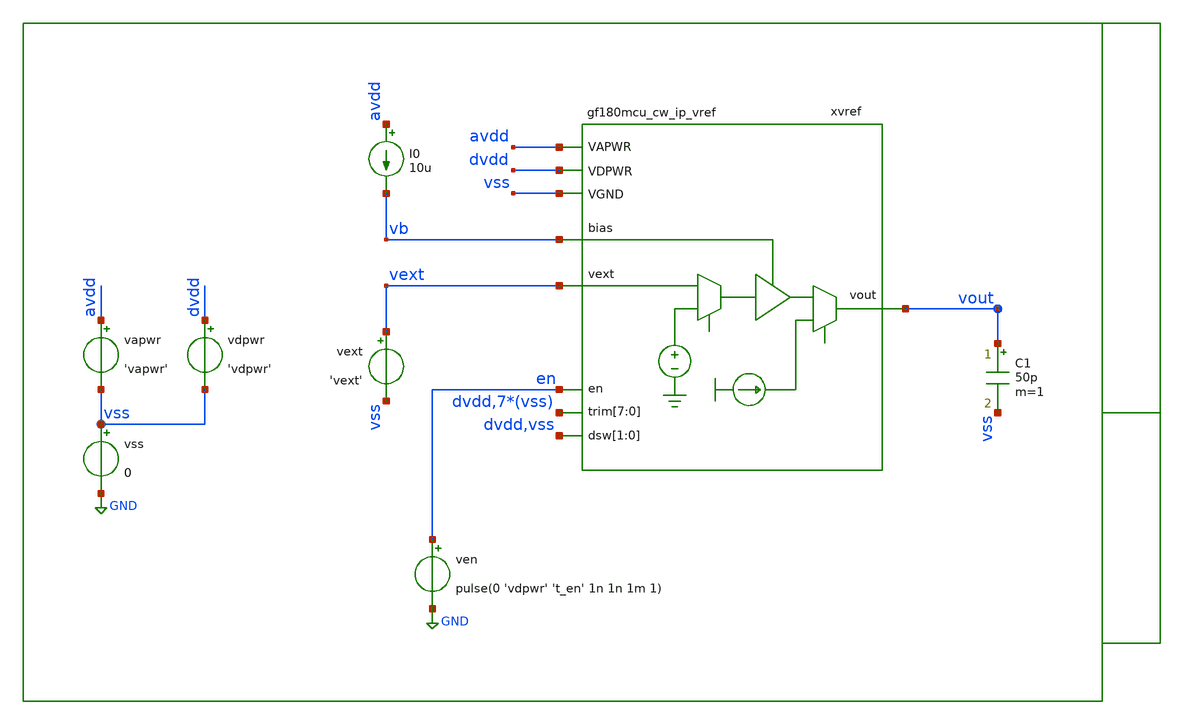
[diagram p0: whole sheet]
** sch_path: xschem/tb/top/tr_gf180mcu_cw_ip_vref.sch
**.subckt tr_gf180mcu_cw_ip_vref
vapwr avdd vss 'vapwr'
vss vss GND 0
vdpwr dvdd vss 'vdpwr'
C1 vout vss 50p m=1
vext vext vss 'vext'
I0 avdd vb 10u
ven en GND pulse(0 'vdpwr' 't_en' 1n 1n 1m 1)
xvref dvdd avdd vb vext vout dvdd vss vss vss vss vss vss vss dvdd vss vss en gf180mcu_cw_ip_vref
**** begin user architecture code

* Control

.temp = 27

.param vapwr = 3.3
.param vdpwr = 3.3
.param vext = 'vapwr/2'

.param t_en = 20u
.csparam t_en = t_en


*.options method  = gear
.options reltol  = 1e-6
*.options abstol  = 1e-12
*.options gmin    = 1e-15

.control

set wr_vecnames
set wr_singlescale

save all
tran 1u 110u uic

let dev = 1

meas tran vout_ss find v(vout) at=100e-6

let lim_pos = vout_ss*(1+dev/100)
let lim_neg = vout_ss*(1-dev/100)

meas tran t_hl when v(vout)=lim_pos fall=last
meas tran t_lh when v(vout)=lim_neg rise=last

let t_set = max(t_hl, t_lh) - t_en

print t_set
print vout_ss

gnuplot p1 en vout lim_pos lim_neg

.endc
.end


 * Model Corners

.include $::CORNERS/ngspice/tt.spice
*.include $::CORNERS/ngspice/ff.spice
*.include $::CORNERS/ngspice/ss.spice
*.include $::CORNERS/ngspice/sf.spice
*.include $::CORNERS/ngspice/fs.spice

**** end user architecture code
**.ends
.GLOBAL GND
.end
